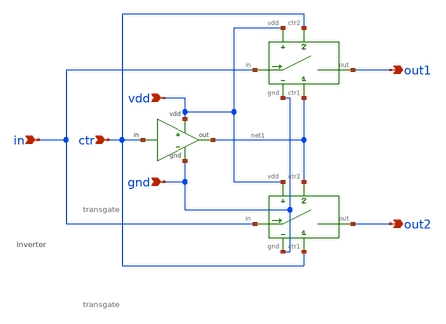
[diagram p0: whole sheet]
** sch_path: xschem/attenuator/spdt.sch
**.subckt spdt in ctr gnd vdd out1 out2
*.ipin in
*.ipin ctr
*.ipin gnd
*.ipin vdd
*.opin out1
*.opin out2
XINV1 vdd ctr gnd net1 inverter
XTG1 vdd ctr in gnd net1 out1 transgate
XTG2 vdd net1 in gnd ctr out2 transgate
XINV1 vdd ctr gnd net1 inverter
**.ends

* expanding   symbol:
*+  /Volumes/WORK_DRIVE/caravel_automatic_gain_control/xschem/attenuator/inverter.sym # of pins=4
** sym_path: xschem/attenuator/inverter.sym
** sch_path: xschem/attenuator/inverter.sch
.subckt inverter vdd in gnd out
*.ipin in
*.ipin gnd
*.ipin vdd
*.opin out
XM1 out in gnd gnd sky130_fd_pr__nfet_01v8 L=0.15 W=4 nf=1 ad='int((nf+1)/2) * W/nf * 0.29' as='int((nf+2)/2) * W/nf * 0.29'
+ pd='2*int((nf+1)/2) * (W/nf + 0.29)' ps='2*int((nf+2)/2) * (W/nf + 0.29)' nrd='0.29 / W' nrs='0.29 / W'
+ sa=0 sb=0 sd=0 mult=1 m=1
XM2 out in vdd vdd sky130_fd_pr__pfet_01v8 L=0.15 W=4 nf=1 ad='int((nf+1)/2) * W/nf * 0.29' as='int((nf+2)/2) * W/nf * 0.29'
+ pd='2*int((nf+1)/2) * (W/nf + 0.29)' ps='2*int((nf+2)/2) * (W/nf + 0.29)' nrd='0.29 / W' nrs='0.29 / W'
+ sa=0 sb=0 sd=0 mult=1 m=1
.ends


* expanding   symbol:
*+  /Volumes/WORK_DRIVE/caravel_automatic_gain_control/xschem/attenuator/transgate.sym # of pins=6
** sym_path: xschem/attenuator/transgate.sym
** sch_path: xschem/attenuator/transgate.sch
.subckt transgate vdd ctr2 in gnd ctr1 out
*.ipin in
*.ipin ctr2
*.ipin ctr1
*.ipin vdd
*.ipin gnd
*.opin out
XM1 in ctr1 out gnd sky130_fd_pr__nfet_01v8 L=0.15 W=4 nf=1 ad='int((nf+1)/2) * W/nf * 0.29' as='int((nf+2)/2) * W/nf * 0.29'
+ pd='2*int((nf+1)/2) * (W/nf + 0.29)' ps='2*int((nf+2)/2) * (W/nf + 0.29)' nrd='0.29 / W' nrs='0.29 / W'
+ sa=0 sb=0 sd=0 mult=1 m=1
XM2 in ctr2 out vdd sky130_fd_pr__pfet_01v8 L=0.15 W=4 nf=1 ad='int((nf+1)/2) * W/nf * 0.29' as='int((nf+2)/2) * W/nf * 0.29'
+ pd='2*int((nf+1)/2) * (W/nf + 0.29)' ps='2*int((nf+2)/2) * (W/nf + 0.29)' nrd='0.29 / W' nrs='0.29 / W'
+ sa=0 sb=0 sd=0 mult=1 m=1
.ends

.end
